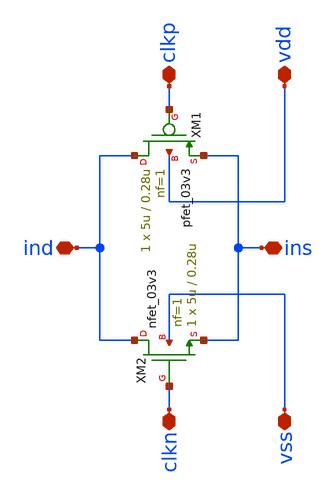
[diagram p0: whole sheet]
** sch_path: designs/libs/qw_core_analog/TG/TG.sch
**.subckt TG ind ins clkn clkp vdd vss
*.iopin ind
*.iopin ins
*.iopin clkn
*.iopin clkp
*.iopin vdd
*.iopin vss
XM1 ind clkp ins vdd pfet_03v3 L=0.28u W=5u nf=1 ad='int((nf+1)/2) * W/nf * 0.18u' as='int((nf+2)/2) * W/nf * 0.18u'
+ pd='2*int((nf+1)/2) * (W/nf + 0.18u)' ps='2*int((nf+2)/2) * (W/nf + 0.18u)' nrd='0.18u / W' nrs='0.18u / W'
+ sa=0 sb=0 sd=0 m=1
XM2 ind clkn ins vss nfet_03v3 L=0.28u W=5u nf=1 ad='int((nf+1)/2) * W/nf * 0.18u' as='int((nf+2)/2) * W/nf * 0.18u'
+ pd='2*int((nf+1)/2) * (W/nf + 0.18u)' ps='2*int((nf+2)/2) * (W/nf + 0.18u)' nrd='0.18u / W' nrs='0.18u / W'
+ sa=0 sb=0 sd=0 m=1
**.ends
.end
